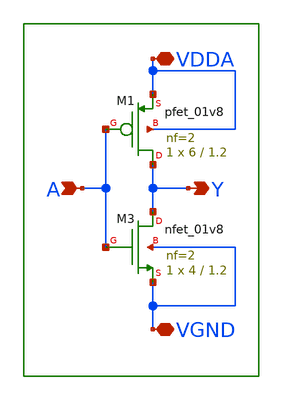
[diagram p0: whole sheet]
** sch_path: xschem/lib/main_inv_dco.sch
**.subckt main_inv_dco VDDA VGND A Y
*.iopin VDDA
*.iopin VGND
*.ipin A
*.opin Y
XM3 Y A VGND VGND sky130_fd_pr__nfet_01v8 L=1.2 W=4 nf=2 ad='int((nf+1)/2) * W/nf * 0.29' as='int((nf+2)/2) * W/nf * 0.29'
+ pd='2*int((nf+1)/2) * (W/nf + 0.29)' ps='2*int((nf+2)/2) * (W/nf + 0.29)' nrd='0.29 / W' nrs='0.29 / W'
+ sa=0 sb=0 sd=0 mult=1 m=1
XM1 Y A VDDA VDDA sky130_fd_pr__pfet_01v8 L=1.2 W=6 nf=2 ad='int((nf+1)/2) * W/nf * 0.29' as='int((nf+2)/2) * W/nf * 0.29'
+ pd='2*int((nf+1)/2) * (W/nf + 0.29)' ps='2*int((nf+2)/2) * (W/nf + 0.29)' nrd='0.29 / W' nrs='0.29 / W'
+ sa=0 sb=0 sd=0 mult=1 m=1
**.ends
.end
